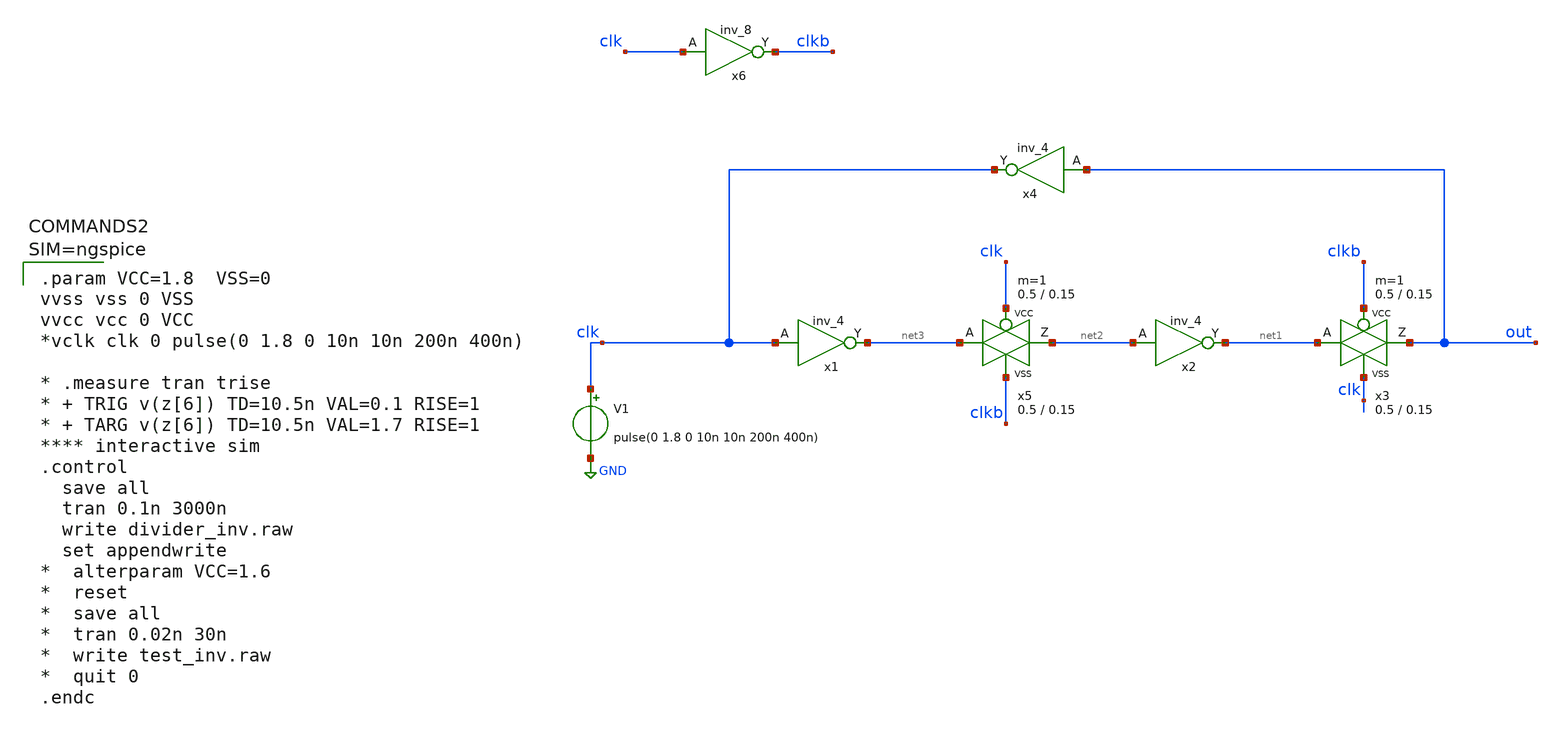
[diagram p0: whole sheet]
** sch_path: xschem/divider/divider_inv.sch
.lib $::SKYWATER_MODELS/sky130.lib.spice tt
.include $::SKYWATER_STDCELLS/sky130_fd_sc_hd.spice

**.subckt divider_inv
V1 clk GND pulse(0 1.8 0 10n 10n 200n 400n)
x5 net2 net3 clk clkb VCC VSS passgate W_N=0.5 L_N=0.15 W_P=0.5 L_P=0.15 m=1
x1 clk VSS VSS VCC VCC net3 sky130_fd_sc_hd__inv_4
x3 out net1 clkb clk VCC VSS passgate W_N=0.5 L_N=0.15 W_P=0.5 L_P=0.15 m=1
x2 net2 VSS VSS VCC VCC net1 sky130_fd_sc_hd__inv_4
x4 out VSS VSS VCC VCC clk sky130_fd_sc_hd__inv_4
x6 clk VSS VSS VCC VCC clkb sky130_fd_sc_hd__inv_8
**** begin user architecture code


.param VCC=1.8  VSS=0
vvss vss 0 VSS
vvcc vcc 0 VCC
*vclk clk 0 pulse(0 1.8 0 10n 10n 200n 400n)

* .measure tran trise
* + TRIG v(z[6]) TD=10.5n VAL=0.1 RISE=1
* + TARG v(z[6]) TD=10.5n VAL=1.7 RISE=1
**** interactive sim
.control
  save all
  tran 0.1n 3000n
  write divider_inv.raw
  set appendwrite
*  alterparam VCC=1.6
*  reset
*  save all
*  tran 0.02n 30n
*  write test_inv.raw
*  quit 0
.endc



**** end user architecture code
**.ends

* expanding   symbol:  sky130_tests/passgate.sym # of pins=4
** sym_path: sky130_tests/passgate.sym
** sch_path: sky130_tests/passgate.sch
.subckt passgate Z A GP GN VCCBPIN VSSBPIN  W_N=1 L_N=0.2 W_P=1 L_P=0.2

*.iopin A
*.iopin Z
*.ipin GP
*.ipin GN
XM1 A GN Z VSS sky130_fd_pr__nfet_01v8 W=W_N L=L_N ad='W * 0.29' pd='W + 2 * 0.29' as='W * 0.29' ps='W + 2 * 0.29'
+ nrd=0 nrs=0 sa=0 sb=0 sd=0 nf=1 mult=1
XM2 A GP Z VCC sky130_fd_pr__pfet_01v8 W=W_P L=L_P ad='W * 0.29' pd='W + 2 * 0.29' as='W * 0.29' ps='W + 2 * 0.29'
+ nrd=0 nrs=0 sa=0 sb=0 sd=0 nf=1 mult=1
.ends

.GLOBAL GND
.end
